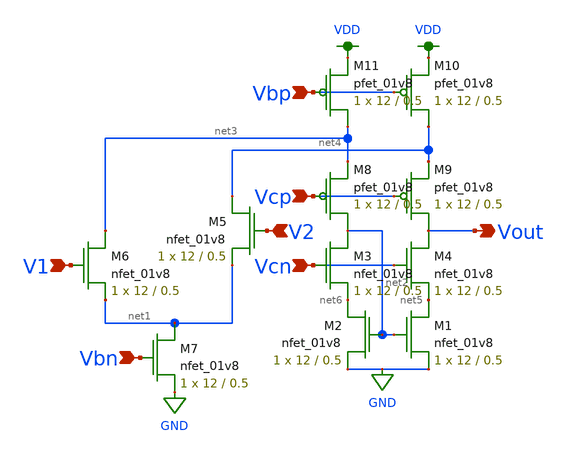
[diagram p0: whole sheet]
** sch_path: mp3/schematics/fcda.sch
**.subckt fcda Vcp V2 Vcn Vbp V1 Vbn Vout
*.ipin Vcp
*.ipin V2
*.ipin Vcn
*.ipin Vbp
*.ipin V1
*.ipin Vbn
*.opin Vout
XM1 net5 net2 GND GND sky130_fd_pr__nfet_01v8 L=0.5 W=12 nf=1 ad='int((nf+1)/2) * W/nf * 0.29' as='int((nf+2)/2) * W/nf * 0.29'
+ pd='2*int((nf+1)/2) * (W/nf + 0.29)' ps='2*int((nf+2)/2) * (W/nf + 0.29)' nrd='0.29 / W' nrs='0.29 / W'
+ sa=0 sb=0 sd=0 mult=1 m=1
XM2 net6 net2 GND GND sky130_fd_pr__nfet_01v8 L=0.5 W=12 nf=1 ad='int((nf+1)/2) * W/nf * 0.29' as='int((nf+2)/2) * W/nf * 0.29'
+ pd='2*int((nf+1)/2) * (W/nf + 0.29)' ps='2*int((nf+2)/2) * (W/nf + 0.29)' nrd='0.29 / W' nrs='0.29 / W'
+ sa=0 sb=0 sd=0 mult=1 m=1
XM3 net2 Vcn net6 GND sky130_fd_pr__nfet_01v8 L=0.5 W=12 nf=1 ad='int((nf+1)/2) * W/nf * 0.29' as='int((nf+2)/2) * W/nf * 0.29'
+ pd='2*int((nf+1)/2) * (W/nf + 0.29)' ps='2*int((nf+2)/2) * (W/nf + 0.29)' nrd='0.29 / W' nrs='0.29 / W'
+ sa=0 sb=0 sd=0 mult=1 m=1
XM4 Vout Vcn net5 GND sky130_fd_pr__nfet_01v8 L=0.5 W=12 nf=1 ad='int((nf+1)/2) * W/nf * 0.29' as='int((nf+2)/2) * W/nf * 0.29'
+ pd='2*int((nf+1)/2) * (W/nf + 0.29)' ps='2*int((nf+2)/2) * (W/nf + 0.29)' nrd='0.29 / W' nrs='0.29 / W'
+ sa=0 sb=0 sd=0 mult=1 m=1
XM5 net4 V2 net1 GND sky130_fd_pr__nfet_01v8 L=0.5 W=12 nf=1 ad='int((nf+1)/2) * W/nf * 0.29' as='int((nf+2)/2) * W/nf * 0.29'
+ pd='2*int((nf+1)/2) * (W/nf + 0.29)' ps='2*int((nf+2)/2) * (W/nf + 0.29)' nrd='0.29 / W' nrs='0.29 / W'
+ sa=0 sb=0 sd=0 mult=1 m=1
XM6 net3 V1 net1 GND sky130_fd_pr__nfet_01v8 L=0.5 W=12 nf=1 ad='int((nf+1)/2) * W/nf * 0.29' as='int((nf+2)/2) * W/nf * 0.29'
+ pd='2*int((nf+1)/2) * (W/nf + 0.29)' ps='2*int((nf+2)/2) * (W/nf + 0.29)' nrd='0.29 / W' nrs='0.29 / W'
+ sa=0 sb=0 sd=0 mult=1 m=1
XM7 net1 Vbn GND GND sky130_fd_pr__nfet_01v8 L=0.5 W=12 nf=1 ad='int((nf+1)/2) * W/nf * 0.29' as='int((nf+2)/2) * W/nf * 0.29'
+ pd='2*int((nf+1)/2) * (W/nf + 0.29)' ps='2*int((nf+2)/2) * (W/nf + 0.29)' nrd='0.29 / W' nrs='0.29 / W'
+ sa=0 sb=0 sd=0 mult=1 m=1
XM8 net2 Vcp net3 VDD sky130_fd_pr__pfet_01v8 L=0.5 W=12 nf=1 ad='int((nf+1)/2) * W/nf * 0.29' as='int((nf+2)/2) * W/nf * 0.29'
+ pd='2*int((nf+1)/2) * (W/nf + 0.29)' ps='2*int((nf+2)/2) * (W/nf + 0.29)' nrd='0.29 / W' nrs='0.29 / W'
+ sa=0 sb=0 sd=0 mult=1 m=1
XM9 Vout Vcp net4 VDD sky130_fd_pr__pfet_01v8 L=0.5 W=12 nf=1 ad='int((nf+1)/2) * W/nf * 0.29' as='int((nf+2)/2) * W/nf * 0.29'
+ pd='2*int((nf+1)/2) * (W/nf + 0.29)' ps='2*int((nf+2)/2) * (W/nf + 0.29)' nrd='0.29 / W' nrs='0.29 / W'
+ sa=0 sb=0 sd=0 mult=1 m=1
XM10 net4 Vbp VDD VDD sky130_fd_pr__pfet_01v8 L=0.5 W=12 nf=1 ad='int((nf+1)/2) * W/nf * 0.29' as='int((nf+2)/2) * W/nf * 0.29'
+ pd='2*int((nf+1)/2) * (W/nf + 0.29)' ps='2*int((nf+2)/2) * (W/nf + 0.29)' nrd='0.29 / W' nrs='0.29 / W'
+ sa=0 sb=0 sd=0 mult=1 m=1
XM11 net3 Vbp VDD VDD sky130_fd_pr__pfet_01v8 L=0.5 W=12 nf=1 ad='int((nf+1)/2) * W/nf * 0.29' as='int((nf+2)/2) * W/nf * 0.29'
+ pd='2*int((nf+1)/2) * (W/nf + 0.29)' ps='2*int((nf+2)/2) * (W/nf + 0.29)' nrd='0.29 / W' nrs='0.29 / W'
+ sa=0 sb=0 sd=0 mult=1 m=1
**.ends
.GLOBAL GND
.GLOBAL VDD
.end
